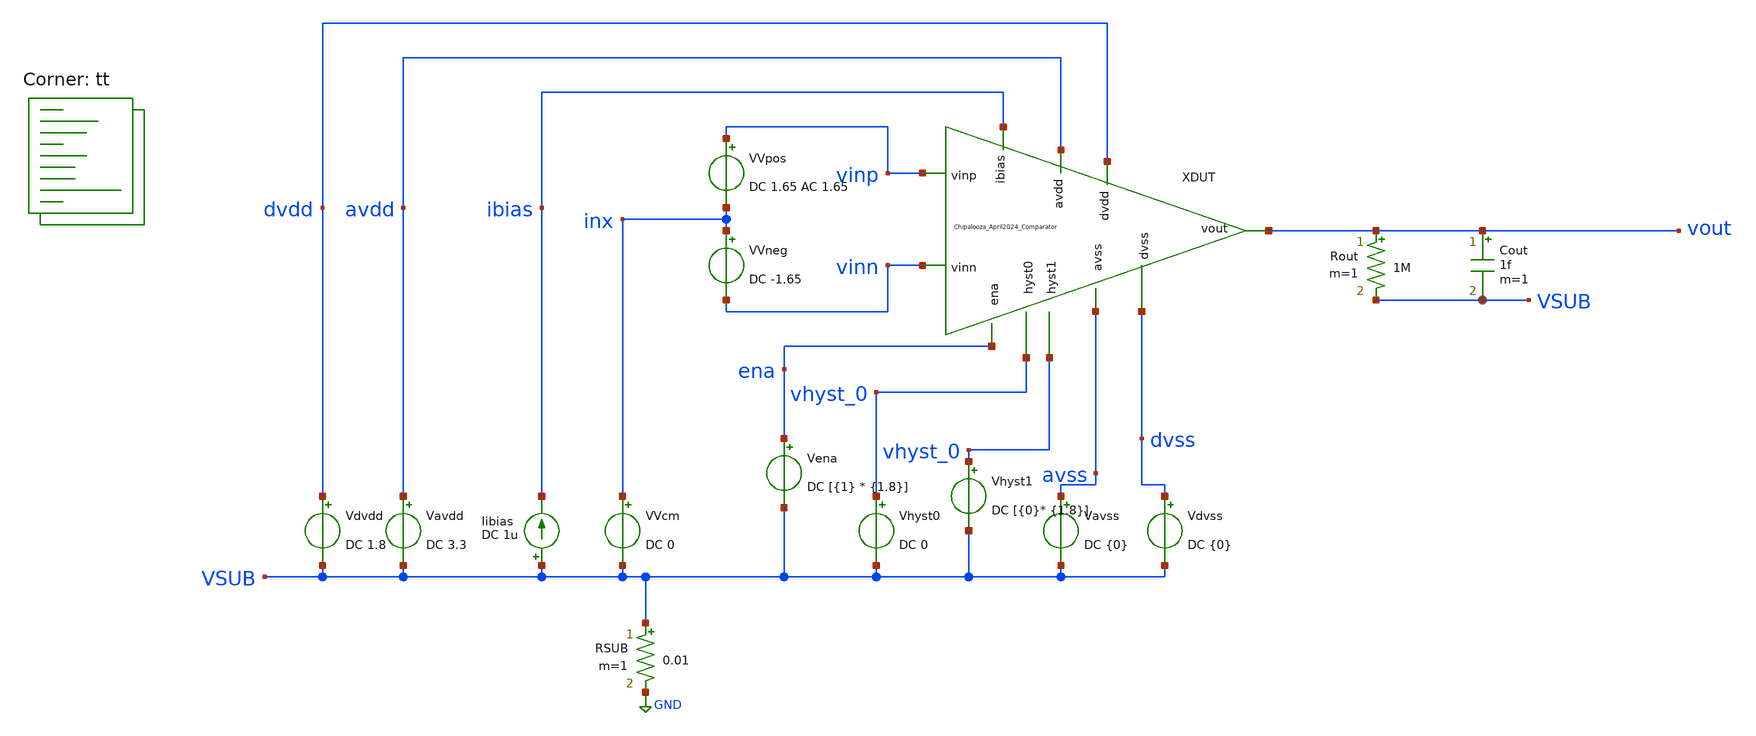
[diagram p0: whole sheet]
** sch_path: Chipalooza_April2024_Comparator/xschem/TB.sch
**.subckt TB
Vavdd avdd VSUB DC 3.3
Rout vout VSUB 1M m=1
Cout vout VSUB 1f m=1
Vdvdd dvdd VSUB DC 1.8
Vena ena VSUB DC [{1} * {1.8}]
Vhyst0 vhyst_0 VSUB DC 0
Vhyst1 vhyst_0 VSUB DC [{0}* {1.8}]
Vavss avss VSUB DC {0}
Vdvss dvss VSUB DC {0}
RSUB VSUB GND 0.01 m=1
Iibias VSUB ibias DC 1u
XDUT vhyst_0 vhyst_0 avdd vinp avss vinn dvdd dvss vout ibias ena Chipalooza_April2024_Comparator
VVpos vinp inx DC 1.65 AC 1.65
VVneg inx vinn DC -1.65
VVcm inx VSUB DC 0
**** begin user architecture code

* this option enables mos model bin
* selection based on W/NF instead of W
*.option wnflag=1
.option savecurrents
.option save all

.control

*Power Consumption
*dc Vinp 0 3.3 0.1
*plot i(v_probe)

*Input Offset Voltage
*op
*plot v(V_offset)

*Propagation Delay
*tran 0.01u 2u
*plot v(vout_pd) v(vin_pd)

*Input Commo-Mode Range
*dc Vin_ICMR 0 3.3 0.1

*Input Capacitance
*tran 0.1u 40u
*plot i(vcap_probe)

*Hyseteresis Bits
*Vhyst_0 Vhyst_0 0 0
*Vhyst_1 Vhyst_0 0 0
*Vhyst_2 Vhyst_0 0 0
*tran 0.1u 100u
*plot v(vin_hyst) v(vout_hyst) v(vhyst0) v(vhyst1) v(vhyst2)
*plot @m.x1.xm5.msky130_fd_pr__nfet_g5v0d10v5[id]

*Frequency Bandwidth
ac dec 20 1 1e12
plot v(vout)
plot v(vhyst_0)
plot v(vinp)

meas ac peak MAX vmag(vout) FROM=2 TO=1GHz
let f3db = peak/sqrt(2)
meas ac f1 when vmag(vout)=f3db RISE=1
meas ac f2 when vmag(vout)=f3db FALL=1


write TB.raw


*quit 0

.endc


.lib $::SKYWATER_MODELS/sky130.lib.spice tt
**** end user architecture code
**.ends

* expanding   symbol:  Chipalooza_April2024_Comparator.sym # of pins=11
** sym_path: Chipalooza_April2024_Comparator/xschem/Chipalooza_April2024_Comparator.sym
** sch_path: Chipalooza_April2024_Comparator/xschem/Chipalooza_April2024_Comparator.sch
.subckt Chipalooza_April2024_Comparator hyst0 hyst1 avdd vinp avss vinn dvdd dvss vout ibias ena
*.ipin vinp
*.ipin vinn
*.ipin hyst0
*.ipin hyst1
*.ipin avdd
*.ipin avss
*.ipin dvdd
*.ipin dvss
*.opin vout
*.ipin ena
*.ipin ibias
XM13 ibias hyst0 net2 dvss sky130_fd_pr__nfet_01v8 L=0.15 W=1 nf=1 ad='int((1 + 1)/2) * 1 / 1 * 0.29'
+ as='int((1 + 2)/2) * 1 / 1 * 0.29' pd='2*int((1 + 1)/2) * (1 / 1 + 0.29)' ps='2*int((1 + 2)/2) * (1 / 1 + 0.29)'
+ nrd='0.29 / 1 ' nrs='0.29 / 1 ' sa=0 sb=0 sd=0 mult=2 m=2
C38 avss 0 2p m=1
XM24 net7 ena avss avss sky130_fd_pr__nfet_g5v0d10v5 L=0.5 W=8 nf=1 ad='int((nf+1)/2) * W/nf * 0.29'
+ as='int((nf+2)/2) * W/nf * 0.29' pd='2*int((nf+1)/2) * (W/nf + 0.29)' ps='2*int((nf+2)/2) * (W/nf + 0.29)'
+ nrd='0.29 / W' nrs='0.29 / W' sa=0 sb=0 sd=0 mult=2 m=2
XM16 ibias hyst1 net1 dvss sky130_fd_pr__nfet_01v8 L=0.15 W=8 nf=1 ad='int((1 + 1)/2) * 8 / 1 * 0.29'
+ as='int((1 + 2)/2) * 8 / 1 * 0.29' pd='2*int((1 + 1)/2) * (8 / 1 + 0.29)' ps='2*int((1 + 2)/2) * (8 / 1 + 0.29)'
+ nrd='0.29 / 8 ' nrs='0.29 / 8 ' sa=0 sb=0 sd=0 mult=2 m=2
XM19 net1 hyst_bias I_hyst dvss sky130_fd_pr__nfet_01v8 L=0.15 W=8 nf=1 ad='int((1 + 1)/2) * 8 / 1 * 0.29'
+ as='int((1 + 2)/2) * 8 / 1 * 0.29' pd='2*int((1 + 1)/2) * (8 / 1 + 0.29)' ps='2*int((1 + 2)/2) * (8 / 1 + 0.29)'
+ nrd='0.29 / 8 ' nrs='0.29 / 8 ' sa=0 sb=0 sd=0 mult=2 m=2
XM18 net2 hyst_bias I_hyst dvss sky130_fd_pr__nfet_01v8 L=0.15 W=1 nf=1 ad='int((1 + 1)/2) * 1 / 1 * 0.29'
+ as='int((1 + 2)/2) * 1 / 1 * 0.29' pd='2*int((1 + 1)/2) * (1 / 1 + 0.29)' ps='2*int((1 + 2)/2) * (1 / 1 + 0.29)'
+ nrd='0.29 / 1 ' nrs='0.29 / 1 ' sa=0 sb=0 sd=0 mult=2 m=2
V1 hyst_bias GND 1.2
XM4 net3 net3 avdd avdd sky130_fd_pr__pfet_g5v0d10v5 L=0.5 W=1 nf=1 ad='int((nf+1)/2) * W/nf * 0.29'
+ as='int((nf+2)/2) * W/nf * 0.29' pd='2*int((nf+1)/2) * (W/nf + 0.29)' ps='2*int((nf+2)/2) * (W/nf + 0.29)'
+ nrd='0.29 / W' nrs='0.29 / W' sa=0 sb=0 sd=0 mult=1 m=1
XM5 N1 net3 avdd avdd sky130_fd_pr__pfet_g5v0d10v5 L=0.5 W=1 nf=1 ad='int((nf+1)/2) * W/nf * 0.29' as='int((nf+2)/2) * W/nf * 0.29'
+ pd='2*int((nf+1)/2) * (W/nf + 0.29)' ps='2*int((nf+2)/2) * (W/nf + 0.29)' nrd='0.29 / W' nrs='0.29 / W'
+ sa=0 sb=0 sd=0 mult=1 m=1
XM6 N2 net3 avdd avdd sky130_fd_pr__pfet_g5v0d10v5 L=0.5 W=1 nf=1 ad='int((nf+1)/2) * W/nf * 0.29' as='int((nf+2)/2) * W/nf * 0.29'
+ pd='2*int((nf+1)/2) * (W/nf + 0.29)' ps='2*int((nf+2)/2) * (W/nf + 0.29)' nrd='0.29 / W' nrs='0.29 / W'
+ sa=0 sb=0 sd=0 mult=1 m=1
XM7 sumOut Bias1 N2 avdd sky130_fd_pr__pfet_g5v0d10v5 L=0.5 W=1 nf=1 ad='int((nf+1)/2) * W/nf * 0.29'
+ as='int((nf+2)/2) * W/nf * 0.29' pd='2*int((nf+1)/2) * (W/nf + 0.29)' ps='2*int((nf+2)/2) * (W/nf + 0.29)'
+ nrd='0.29 / W' nrs='0.29 / W' sa=0 sb=0 sd=0 mult=1 m=1
XM8 net4 Bias1 N1 avdd sky130_fd_pr__pfet_g5v0d10v5 L=0.5 W=1 nf=1 ad='int((nf+1)/2) * W/nf * 0.29' as='int((nf+2)/2) * W/nf * 0.29'
+ pd='2*int((nf+1)/2) * (W/nf + 0.29)' ps='2*int((nf+2)/2) * (W/nf + 0.29)' nrd='0.29 / W' nrs='0.29 / W'
+ sa=0 sb=0 sd=0 mult=1 m=1
XM9 sumOut Bias2 P2 avss sky130_fd_pr__nfet_g5v0d10v5 L=0.5 W=1 nf=1 ad='int((nf+1)/2) * W/nf * 0.29'
+ as='int((nf+2)/2) * W/nf * 0.29' pd='2*int((nf+1)/2) * (W/nf + 0.29)' ps='2*int((nf+2)/2) * (W/nf + 0.29)'
+ nrd='0.29 / W' nrs='0.29 / W' sa=0 sb=0 sd=0 mult=1 m=1
XM10 net4 Bias2 P1 avss sky130_fd_pr__nfet_g5v0d10v5 L=0.5 W=1 nf=1 ad='int((nf+1)/2) * W/nf * 0.29'
+ as='int((nf+2)/2) * W/nf * 0.29' pd='2*int((nf+1)/2) * (W/nf + 0.29)' ps='2*int((nf+2)/2) * (W/nf + 0.29)'
+ nrd='0.29 / W' nrs='0.29 / W' sa=0 sb=0 sd=0 mult=1 m=1
XM11 P2 net4 avss avss sky130_fd_pr__nfet_g5v0d10v5 L=0.5 W=1 nf=1 ad='int((nf+1)/2) * W/nf * 0.29' as='int((nf+2)/2) * W/nf * 0.29'
+ pd='2*int((nf+1)/2) * (W/nf + 0.29)' ps='2*int((nf+2)/2) * (W/nf + 0.29)' nrd='0.29 / W' nrs='0.29 / W'
+ sa=0 sb=0 sd=0 mult=1 m=1
XM12 P1 net4 avss avss sky130_fd_pr__nfet_g5v0d10v5 L=0.5 W=1 nf=1 ad='int((nf+1)/2) * W/nf * 0.29' as='int((nf+2)/2) * W/nf * 0.29'
+ pd='2*int((nf+1)/2) * (W/nf + 0.29)' ps='2*int((nf+2)/2) * (W/nf + 0.29)' nrd='0.29 / W' nrs='0.29 / W'
+ sa=0 sb=0 sd=0 mult=1 m=1
I1 net3 avss 1u
XM1 P2 vinn psource_input avdd sky130_fd_pr__pfet_g5v0d10v5 L=0.5 W=1 nf=1 ad='int((nf+1)/2) * W/nf * 0.29'
+ as='int((nf+2)/2) * W/nf * 0.29' pd='2*int((nf+1)/2) * (W/nf + 0.29)' ps='2*int((nf+2)/2) * (W/nf + 0.29)'
+ nrd='0.29 / W' nrs='0.29 / W' sa=0 sb=0 sd=0 mult=1 m=1
XM2 P1 vinp psource_input avdd sky130_fd_pr__pfet_g5v0d10v5 L=0.5 W=1 nf=1 ad='int((nf+1)/2) * W/nf * 0.29'
+ as='int((nf+2)/2) * W/nf * 0.29' pd='2*int((nf+1)/2) * (W/nf + 0.29)' ps='2*int((nf+2)/2) * (W/nf + 0.29)'
+ nrd='0.29 / W' nrs='0.29 / W' sa=0 sb=0 sd=0 mult=1 m=1
I2 avdd psource_input 0.5u
XM3 psource_input net5 avdd avdd sky130_fd_pr__pfet_g5v0d10v5 L=0.5 W=3 nf=1 ad='int((nf+1)/2) * W/nf * 0.29'
+ as='int((nf+2)/2) * W/nf * 0.29' pd='2*int((nf+1)/2) * (W/nf + 0.29)' ps='2*int((nf+2)/2) * (W/nf + 0.29)'
+ nrd='0.29 / W' nrs='0.29 / W' sa=0 sb=0 sd=0 mult=1 m=1
XM14 net5 net5 avdd avdd sky130_fd_pr__pfet_g5v0d10v5 L=0.5 W=1 nf=1 ad='int((nf+1)/2) * W/nf * 0.29'
+ as='int((nf+2)/2) * W/nf * 0.29' pd='2*int((nf+1)/2) * (W/nf + 0.29)' ps='2*int((nf+2)/2) * (W/nf + 0.29)'
+ nrd='0.29 / W' nrs='0.29 / W' sa=0 sb=0 sd=0 mult=1 m=1
XM15 net6 Pbias psource_input avdd sky130_fd_pr__pfet_g5v0d10v5 L=0.5 W=1 nf=1 ad='int((nf+1)/2) * W/nf * 0.29'
+ as='int((nf+2)/2) * W/nf * 0.29' pd='2*int((nf+1)/2) * (W/nf + 0.29)' ps='2*int((nf+2)/2) * (W/nf + 0.29)'
+ nrd='0.29 / W' nrs='0.29 / W' sa=0 sb=0 sd=0 mult=1 m=1
XM17 N1 vinp ndrain_input avss sky130_fd_pr__nfet_g5v0d10v5 L=0.5 W=1 nf=1 ad='int((nf+1)/2) * W/nf * 0.29'
+ as='int((nf+2)/2) * W/nf * 0.29' pd='2*int((nf+1)/2) * (W/nf + 0.29)' ps='2*int((nf+2)/2) * (W/nf + 0.29)'
+ nrd='0.29 / W' nrs='0.29 / W' sa=0 sb=0 sd=0 mult=1 m=1
XM20 N2 vinn ndrain_input avss sky130_fd_pr__nfet_g5v0d10v5 L=0.5 W=1 nf=1 ad='int((nf+1)/2) * W/nf * 0.29'
+ as='int((nf+2)/2) * W/nf * 0.29' pd='2*int((nf+1)/2) * (W/nf + 0.29)' ps='2*int((nf+2)/2) * (W/nf + 0.29)'
+ nrd='0.29 / W' nrs='0.29 / W' sa=0 sb=0 sd=0 mult=1 m=1
XM21 ndrain_input net6 net7 avss sky130_fd_pr__nfet_g5v0d10v5 L=0.5 W=3 nf=1 ad='int((nf+1)/2) * W/nf * 0.29'
+ as='int((nf+2)/2) * W/nf * 0.29' pd='2*int((nf+1)/2) * (W/nf + 0.29)' ps='2*int((nf+2)/2) * (W/nf + 0.29)'
+ nrd='0.29 / W' nrs='0.29 / W' sa=0 sb=0 sd=0 mult=1 m=1
XM22 net6 net6 net7 avss sky130_fd_pr__nfet_g5v0d10v5 L=0.5 W=1 nf=1 ad='int((nf+1)/2) * W/nf * 0.29'
+ as='int((nf+2)/2) * W/nf * 0.29' pd='2*int((nf+1)/2) * (W/nf + 0.29)' ps='2*int((nf+2)/2) * (W/nf + 0.29)'
+ nrd='0.29 / W' nrs='0.29 / W' sa=0 sb=0 sd=0 mult=1 m=1
I3 ndrain_input net7 0.5u
XM23 net5 Nbias ndrain_input avss sky130_fd_pr__nfet_g5v0d10v5 L=0.5 W=1 nf=1 ad='int((nf+1)/2) * W/nf * 0.29'
+ as='int((nf+2)/2) * W/nf * 0.29' pd='2*int((nf+1)/2) * (W/nf + 0.29)' ps='2*int((nf+2)/2) * (W/nf + 0.29)'
+ nrd='0.29 / W' nrs='0.29 / W' sa=0 sb=0 sd=0 mult=1 m=1
V2 Bias1 avss 2
V3 Bias2 avss 1.65
V4 Pbias avss 1.65
V5 Nbias avss 1.65
XM29 net8 sumOut dvdd dvdd sky130_fd_pr__pfet_01v8 L=0.15 W=1 nf=1 ad='int((nf+1)/2) * W/nf * 0.29' as='int((nf+2)/2) * W/nf * 0.29'
+ pd='2*int((nf+1)/2) * (W/nf + 0.29)' ps='2*int((nf+2)/2) * (W/nf + 0.29)' nrd='0.29 / W' nrs='0.29 / W'
+ sa=0 sb=0 sd=0 mult=1 m=1
XM30 net8 sumOut dvss dvss sky130_fd_pr__nfet_01v8 L=0.15 W=1 nf=1 ad='int((nf+1)/2) * W/nf * 0.29' as='int((nf+2)/2) * W/nf * 0.29'
+ pd='2*int((nf+1)/2) * (W/nf + 0.29)' ps='2*int((nf+2)/2) * (W/nf + 0.29)' nrd='0.29 / W' nrs='0.29 / W'
+ sa=0 sb=0 sd=0 mult=1 m=1
XM31 vout net8 dvdd dvdd sky130_fd_pr__pfet_01v8 L=0.15 W=1 nf=1 ad='int((nf+1)/2) * W/nf * 0.29' as='int((nf+2)/2) * W/nf * 0.29'
+ pd='2*int((nf+1)/2) * (W/nf + 0.29)' ps='2*int((nf+2)/2) * (W/nf + 0.29)' nrd='0.29 / W' nrs='0.29 / W'
+ sa=0 sb=0 sd=0 mult=1 m=1
XM32 vout net8 dvss dvss sky130_fd_pr__nfet_01v8 L=0.15 W=1 nf=1 ad='int((nf+1)/2) * W/nf * 0.29' as='int((nf+2)/2) * W/nf * 0.29'
+ pd='2*int((nf+1)/2) * (W/nf + 0.29)' ps='2*int((nf+2)/2) * (W/nf + 0.29)' nrd='0.29 / W' nrs='0.29 / W'
+ sa=0 sb=0 sd=0 mult=1 m=1
.ends

.GLOBAL GND
.end
